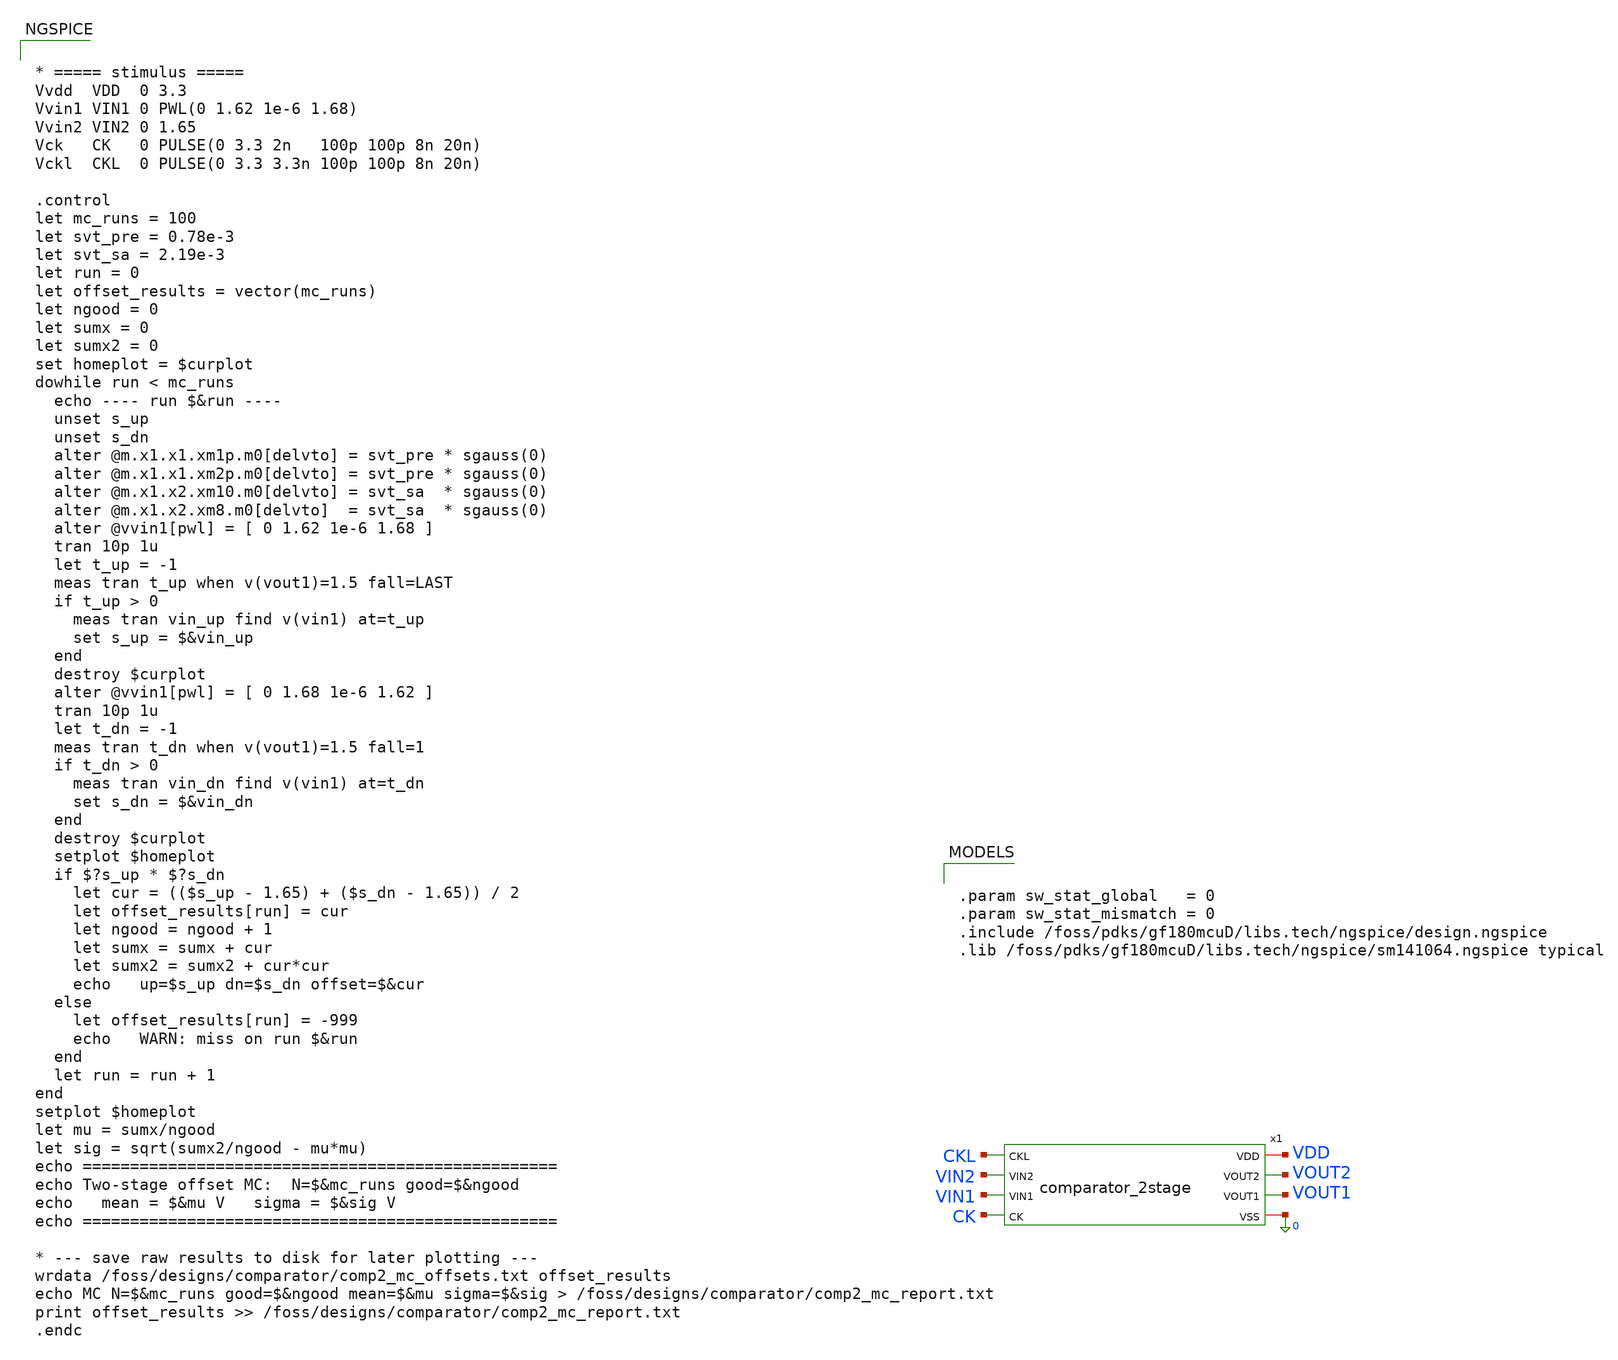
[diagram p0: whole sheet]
** sch_path: comparator/schematic/tb_2stage.sch
**.subckt tb_2stage
x1 CKL VIN2 VDD VOUT2 VIN1 VOUT1 CK 0 comparator_2stage
**** begin user architecture code


.param sw_stat_global   = 0
.param sw_stat_mismatch = 0
.include /foss/pdks/gf180mcuD/libs.tech/ngspice/design.ngspice
.lib /foss/pdks/gf180mcuD/libs.tech/ngspice/sm141064.ngspice typical




* ===== stimulus =====
Vvdd  VDD  0 3.3
Vvin1 VIN1 0 PWL(0 1.62 1e-6 1.68)
Vvin2 VIN2 0 1.65
Vck   CK   0 PULSE(0 3.3 2n   100p 100p 8n 20n)
Vckl  CKL  0 PULSE(0 3.3 3.3n 100p 100p 8n 20n)

.control
let mc_runs = 100
let svt_pre = 0.78e-3
let svt_sa = 2.19e-3
let run = 0
let offset_results = vector(mc_runs)
let ngood = 0
let sumx = 0
let sumx2 = 0
set homeplot = $curplot
dowhile run < mc_runs
  echo ---- run $&run ----
  unset s_up
  unset s_dn
  alter @m.x1.x1.xm1p.m0[delvto] = svt_pre * sgauss(0)
  alter @m.x1.x1.xm2p.m0[delvto] = svt_pre * sgauss(0)
  alter @m.x1.x2.xm10.m0[delvto] = svt_sa  * sgauss(0)
  alter @m.x1.x2.xm8.m0[delvto]  = svt_sa  * sgauss(0)
  alter @vvin1[pwl] = [ 0 1.62 1e-6 1.68 ]
  tran 10p 1u
  let t_up = -1
  meas tran t_up when v(vout1)=1.5 fall=LAST
  if t_up > 0
    meas tran vin_up find v(vin1) at=t_up
    set s_up = $&vin_up
  end
  destroy $curplot
  alter @vvin1[pwl] = [ 0 1.68 1e-6 1.62 ]
  tran 10p 1u
  let t_dn = -1
  meas tran t_dn when v(vout1)=1.5 fall=1
  if t_dn > 0
    meas tran vin_dn find v(vin1) at=t_dn
    set s_dn = $&vin_dn
  end
  destroy $curplot
  setplot $homeplot
  if $?s_up * $?s_dn
    let cur = (($s_up - 1.65) + ($s_dn - 1.65)) / 2
    let offset_results[run] = cur
    let ngood = ngood + 1
    let sumx = sumx + cur
    let sumx2 = sumx2 + cur*cur
    echo   up=$s_up dn=$s_dn offset=$&cur
  else
    let offset_results[run] = -999
    echo   WARN: miss on run $&run
  end
  let run = run + 1
end
setplot $homeplot
let mu = sumx/ngood
let sig = sqrt(sumx2/ngood - mu*mu)
echo ==================================================
echo Two-stage offset MC:  N=$&mc_runs good=$&ngood
echo   mean = $&mu V   sigma = $&sig V
echo ==================================================

* --- save raw results to disk for later plotting ---
wrdata /foss/designs/comparator/comp2_mc_offsets.txt offset_results
echo MC N=$&mc_runs good=$&ngood mean=$&mu sigma=$&sig >
+ /foss/designs/comparator/comp2_mc_report.txt
print offset_results >> /foss/designs/comparator/comp2_mc_report.txt
.endc


**** end user architecture code
**.ends
.end
